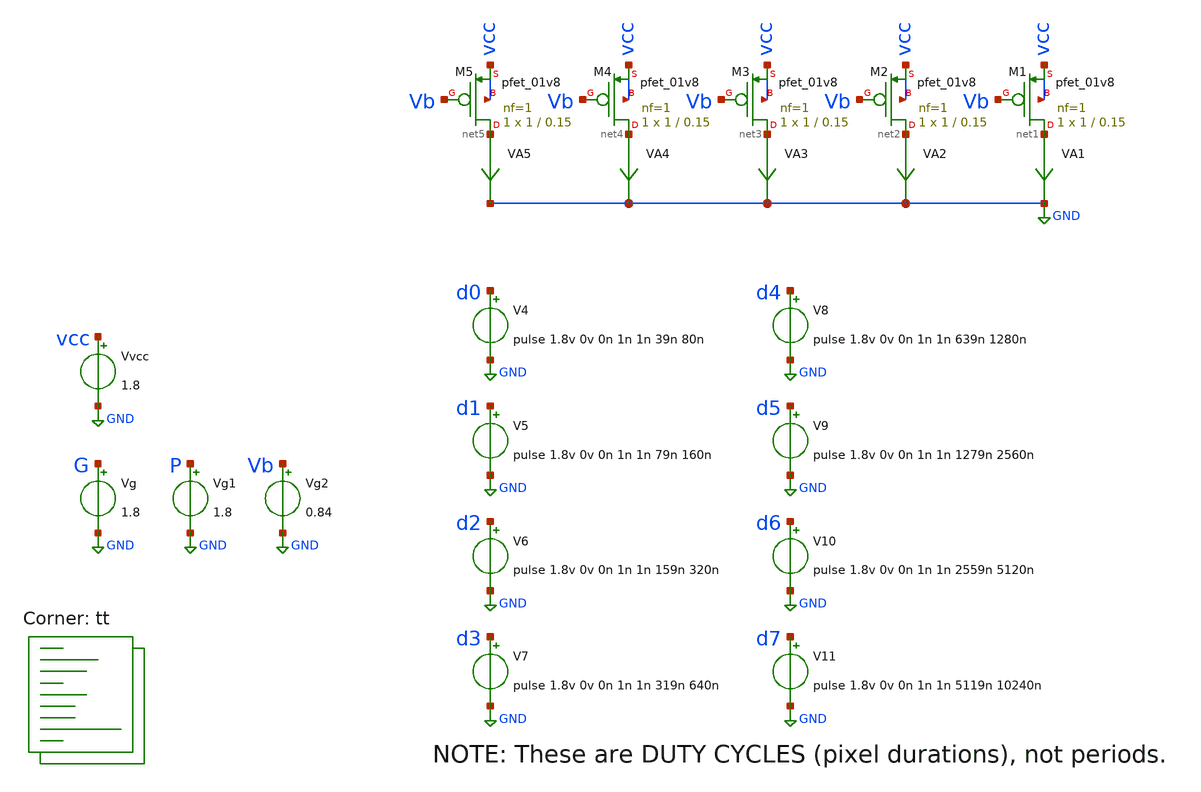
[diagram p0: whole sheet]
** sch_path: xschem/07-mixed.sch
**.subckt 07-mixed
Vvcc vcc GND 1.8
Vg G GND 1.8
V4 d0 GND pulse 1.8v 0v 0n 1n 1n 39n 80n
V5 d1 GND pulse 1.8v 0v 0n 1n 1n 79n 160n
V6 d2 GND pulse 1.8v 0v 0n 1n 1n 159n 320n
V7 d3 GND pulse 1.8v 0v 0n 1n 1n 319n 640n
V8 d4 GND pulse 1.8v 0v 0n 1n 1n 639n 1280n
V9 d5 GND pulse 1.8v 0v 0n 1n 1n 1279n 2560n
V10 d6 GND pulse 1.8v 0v 0n 1n 1n 2559n 5120n
V11 d7 GND pulse 1.8v 0v 0n 1n 1n 5119n 10240n
Vg1 P GND 1.8
XM1 net1 Vb vcc vcc sky130_fd_pr__pfet_01v8 L=0.15 W=1 nf=1 ad='int((nf+1)/2) * W/nf * 0.29' as='int((nf+2)/2) * W/nf * 0.29'
+ pd='2*int((nf+1)/2) * (W/nf + 0.29)' ps='2*int((nf+2)/2) * (W/nf + 0.29)' nrd='0.29 / W' nrs='0.29 / W'
+ sa=0 sb=0 sd=0 mult=1 m=1
XM2 net2 Vb vcc vcc sky130_fd_pr__pfet_01v8 L=0.15 W=1 nf=1 ad='int((nf+1)/2) * W/nf * 0.29' as='int((nf+2)/2) * W/nf * 0.29'
+ pd='2*int((nf+1)/2) * (W/nf + 0.29)' ps='2*int((nf+2)/2) * (W/nf + 0.29)' nrd='0.29 / W' nrs='0.29 / W'
+ sa=0 sb=0 sd=0 mult=1 m=1
XM3 net3 Vb vcc vcc sky130_fd_pr__pfet_01v8 L=0.15 W=1 nf=1 ad='int((nf+1)/2) * W/nf * 0.29' as='int((nf+2)/2) * W/nf * 0.29'
+ pd='2*int((nf+1)/2) * (W/nf + 0.29)' ps='2*int((nf+2)/2) * (W/nf + 0.29)' nrd='0.29 / W' nrs='0.29 / W'
+ sa=0 sb=0 sd=0 mult=1 m=1
XM4 net4 Vb vcc vcc sky130_fd_pr__pfet_01v8 L=0.15 W=1 nf=1 ad='int((nf+1)/2) * W/nf * 0.29' as='int((nf+2)/2) * W/nf * 0.29'
+ pd='2*int((nf+1)/2) * (W/nf + 0.29)' ps='2*int((nf+2)/2) * (W/nf + 0.29)' nrd='0.29 / W' nrs='0.29 / W'
+ sa=0 sb=0 sd=0 mult=1 m=1
XM5 net5 Vb vcc vcc sky130_fd_pr__pfet_01v8 L=0.15 W=1 nf=1 ad='int((nf+1)/2) * W/nf * 0.29' as='int((nf+2)/2) * W/nf * 0.29'
+ pd='2*int((nf+1)/2) * (W/nf + 0.29)' ps='2*int((nf+2)/2) * (W/nf + 0.29)' nrd='0.29 / W' nrs='0.29 / W'
+ sa=0 sb=0 sd=0 mult=1 m=1
VA1 net1 GND 0
.save i(va1)
VA2 net2 GND 0
.save i(va2)
VA3 net3 GND 0
.save i(va3)
VA4 net4 GND 0
.save i(va4)
VA5 net5 GND 0
.save i(va5)
Vg2 Vb GND 0.84
**** begin user architecture code



.options savecurrents
.control

  save all
  tran 1n 12.8u
  write 07.raw v(Vb) i(va1) i(va2) i(va3) i(va4) i(va5)
  plot i(va1) i(va2) i(va3) i(va4) i(va5)

.endc



.lib $::SKYWATER_MODELS/sky130.lib.spice tt
**** end user architecture code
**.ends
.GLOBAL GND
.end
